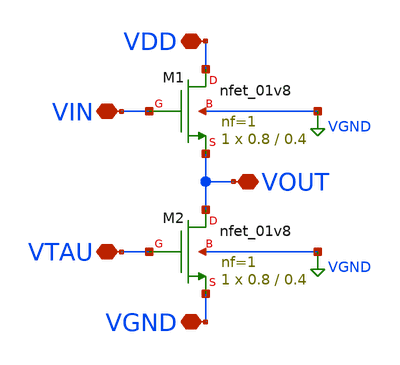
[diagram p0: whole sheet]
** sch_path: project2/source_follower/source_follower.sch
**.subckt source_follower VIN VTAU VOUT VDD VGND
*.iopin VIN
*.iopin VTAU
*.iopin VOUT
*.iopin VDD
*.iopin VGND
XM1 VDD VIN VOUT VGND sky130_fd_pr__nfet_01v8 L=0.4 W=0.8 nf=1 ad='int((nf+1)/2) * W/nf * 0.29' as='int((nf+2)/2) * W/nf * 0.29'
+ pd='2*int((nf+1)/2) * (W/nf + 0.29)' ps='2*int((nf+2)/2) * (W/nf + 0.29)' nrd='0.29 / W' nrs='0.29 / W'
+ sa=0 sb=0 sd=0 mult=1 m=1
XM2 VOUT VTAU VGND VGND sky130_fd_pr__nfet_01v8 L=0.4 W=0.8 nf=1 ad='int((nf+1)/2) * W/nf * 0.29' as='int((nf+2)/2) * W/nf * 0.29'
+ pd='2*int((nf+1)/2) * (W/nf + 0.29)' ps='2*int((nf+2)/2) * (W/nf + 0.29)' nrd='0.29 / W' nrs='0.29 / W'
+ sa=0 sb=0 sd=0 mult=1 m=1
**.ends
.GLOBAL VGND
.end
